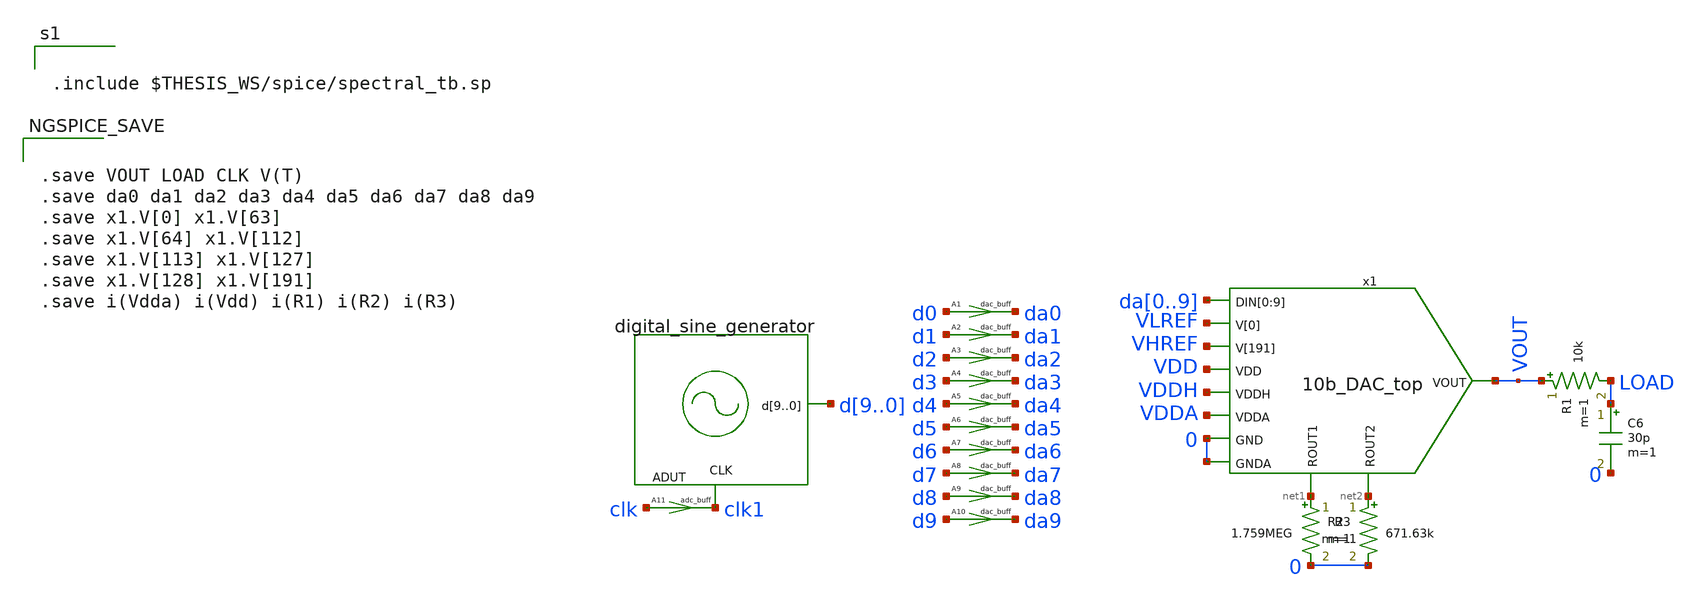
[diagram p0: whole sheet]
** sch_path: xschem/10b_DAC_spectral-tb.sch
.lib $::SKYWATER_MODELS/sky130.lib.spice tt
.include $::SKYWATER_STDCELLS/sky130_fd_sc_hd.spice
.include ~/pdk/sky130A/libs.ref/sky130_fd_sc_hvl/spice/sky130_fd_sc_hvl.spice

**.subckt 10b_DAC_spectral-tb
A1 [ d0 ] [ da0 ] dac_buff
A2 [ d1 ] [ da1 ] dac_buff
A3 [ d2 ] [ da2 ] dac_buff
A4 [ d3 ] [ da3 ] dac_buff
A5 [ d4 ] [ da4 ] dac_buff
A6 [ d5 ] [ da5 ] dac_buff
A7 [ d6 ] [ da6 ] dac_buff
A8 [ d7 ] [ da7 ] dac_buff
A9 [ d8 ] [ da8 ] dac_buff
A10 [ d9 ] [ da9 ] dac_buff
A11 [ clk ] [ clk1 ] adc_buff
C6 LOAD 0 30p m=1
R1 VOUT LOAD 10k m=1
x1 da0 da1 da2 da3 da4 da5 da6 da7 da8 da9 VLREF VHREF VDD VDDH VDDA 0 0 VOUT net1 net2 10b_DAC_top
ADUT [ clk1 ] [ d9 d8 d7 d6 d5 d4 d3 d2 d1 d0 ] digital_sine_generator
R2 net1 0 1.759MEG m=1
R3 net2 0 671.63k m=1
**** begin user architecture code


.include $THESIS_WS/spice/spectral_tb.sp



.save VOUT LOAD CLK V(T)
.save da0 da1 da2 da3 da4 da5 da6 da7 da8 da9
.save x1.V[0] x1.V[63]
.save x1.V[64] x1.V[112]
.save x1.V[113] x1.V[127]
.save x1.V[128] x1.V[191]
.save i(Vdda) i(Vdd) i(R1) i(R2) i(R3)


**** end user architecture code
**.ends
**** begin user architecture code
.model digital_sine_generator d_cosim simulation="ivlng" sim_args=["dsine_gen"]
**** end user architecture code
.end
